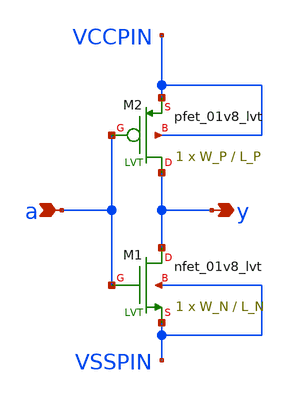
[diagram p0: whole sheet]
** sch_path: xyce/sky130A-xyce/libs.tech/xschem/sky130_tests/lvtnot.sch
* Copyright 2020 Stefan Frederik Schippers
* Licensed under the Apache License, Version 2.0 (the "License");
* you may not use this file except in compliance with the License.
* You may obtain a copy of the License at
* https://www.apache.org/licenses/LICENSE-2.0
* Unless required by applicable law or agreed to in writing, software
* distributed under the License is distributed on an "AS IS" BASIS,
* WITHOUT WARRANTIES OR CONDITIONS OF ANY KIND, either express or implied.
* See the License for the specific language governing permissions and
* limitations under the License.
**.subckt lvtnot y a
*.opin y
*.ipin a
XM2 y a VCCPIN VCCPIN sky130_fd_pr__pfet_01v8_lvt L=L_P W=W_P nf=1 ad='int((nf+1)/2) * W/nf * 0.29' as='int((nf+2)/2) * W/nf * 0.29'
+ pd='2*int((nf+1)/2) * (W/nf + 0.29)' ps='2*int((nf+2)/2) * (W/nf + 0.29)' nrd='0.29 / W' nrs='0.29 / W'
+ sa=0 sb=0 sd=0 mult=1 m=1
XM1 y a VSSPIN VSSPIN sky130_fd_pr__nfet_01v8_lvt L=L_N W=W_N nf=1 ad='int((nf+1)/2) * W/nf * 0.29' as='int((nf+2)/2) * W/nf * 0.29'
+ pd='2*int((nf+1)/2) * (W/nf + 0.29)' ps='2*int((nf+2)/2) * (W/nf + 0.29)' nrd='0.29 / W' nrs='0.29 / W'
+ sa=0 sb=0 sd=0 mult=1 m=1
**.ends
.end
